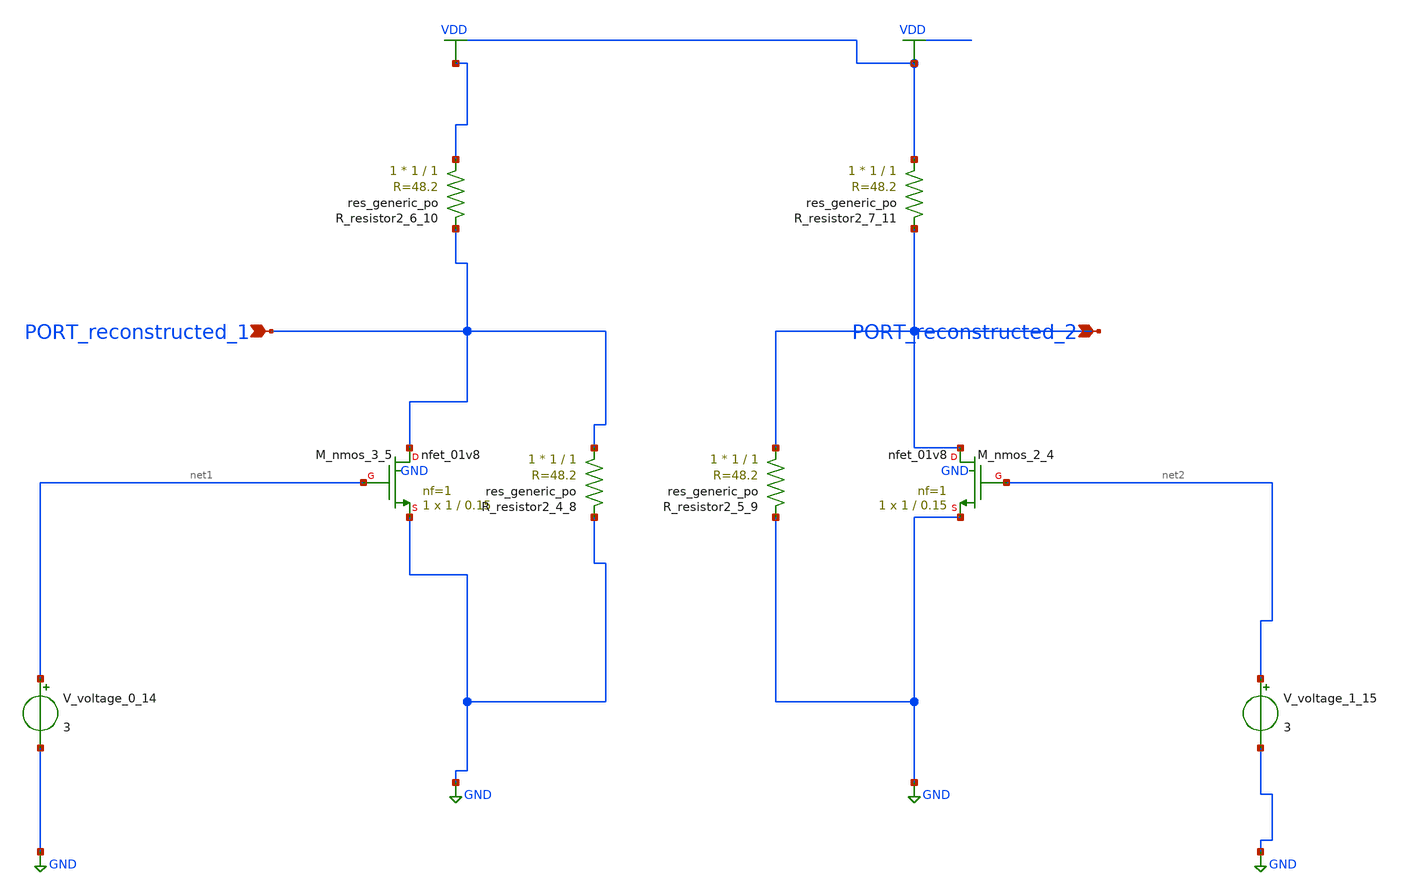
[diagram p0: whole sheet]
** sch_path: schematics/AMSNet/205.sch
**.subckt 205 PORT_reconstructed_1 PORT_reconstructed_2
*.ipin PORT_reconstructed_1
*.ipin PORT_reconstructed_2
XM_nmos_2_4 PORT_reconstructed_2 net2 GND GND sky130_fd_pr__nfet_01v8 L=0.15 W=1 nf=1 ad='int((1 + 1)/2) * 1 / 1 * 0.29'
+ as='int((1 + 2)/2) * 1 / 1 * 0.29' pd='2*int((1 + 1)/2) * (1 / 1 + 0.29)' ps='2*int((1 + 2)/2) * (1 / 1 + 0.29)'
+ nrd='0.29 / 1 ' nrs='0.29 / 1 ' sa=0 sb=0 sd=0 mult=1 m=1
XM_nmos_3_5 PORT_reconstructed_1 net1 GND GND sky130_fd_pr__nfet_01v8 L=0.15 W=1 nf=1 ad='int((1 + 1)/2) * 1 / 1 * 0.29'
+ as='int((1 + 2)/2) * 1 / 1 * 0.29' pd='2*int((1 + 1)/2) * (1 / 1 + 0.29)' ps='2*int((1 + 2)/2) * (1 / 1 + 0.29)'
+ nrd='0.29 / 1 ' nrs='0.29 / 1 ' sa=0 sb=0 sd=0 mult=1 m=1
XR_resistor2_4_8 PORT_reconstructed_1 GND sky130_fd_pr__res_generic_po W=1 L=1 m=1
XR_resistor2_5_9 PORT_reconstructed_2 GND sky130_fd_pr__res_generic_po W=1 L=1 m=1
XR_resistor2_6_10 VDD PORT_reconstructed_1 sky130_fd_pr__res_generic_po W=1 L=1 m=1
XR_resistor2_7_11 VDD PORT_reconstructed_2 sky130_fd_pr__res_generic_po W=1 L=1 m=1
V_voltage_0_14 net1 GND 3
V_voltage_1_15 net2 GND 3
**.ends
.GLOBAL GND
.GLOBAL VDD
.end
